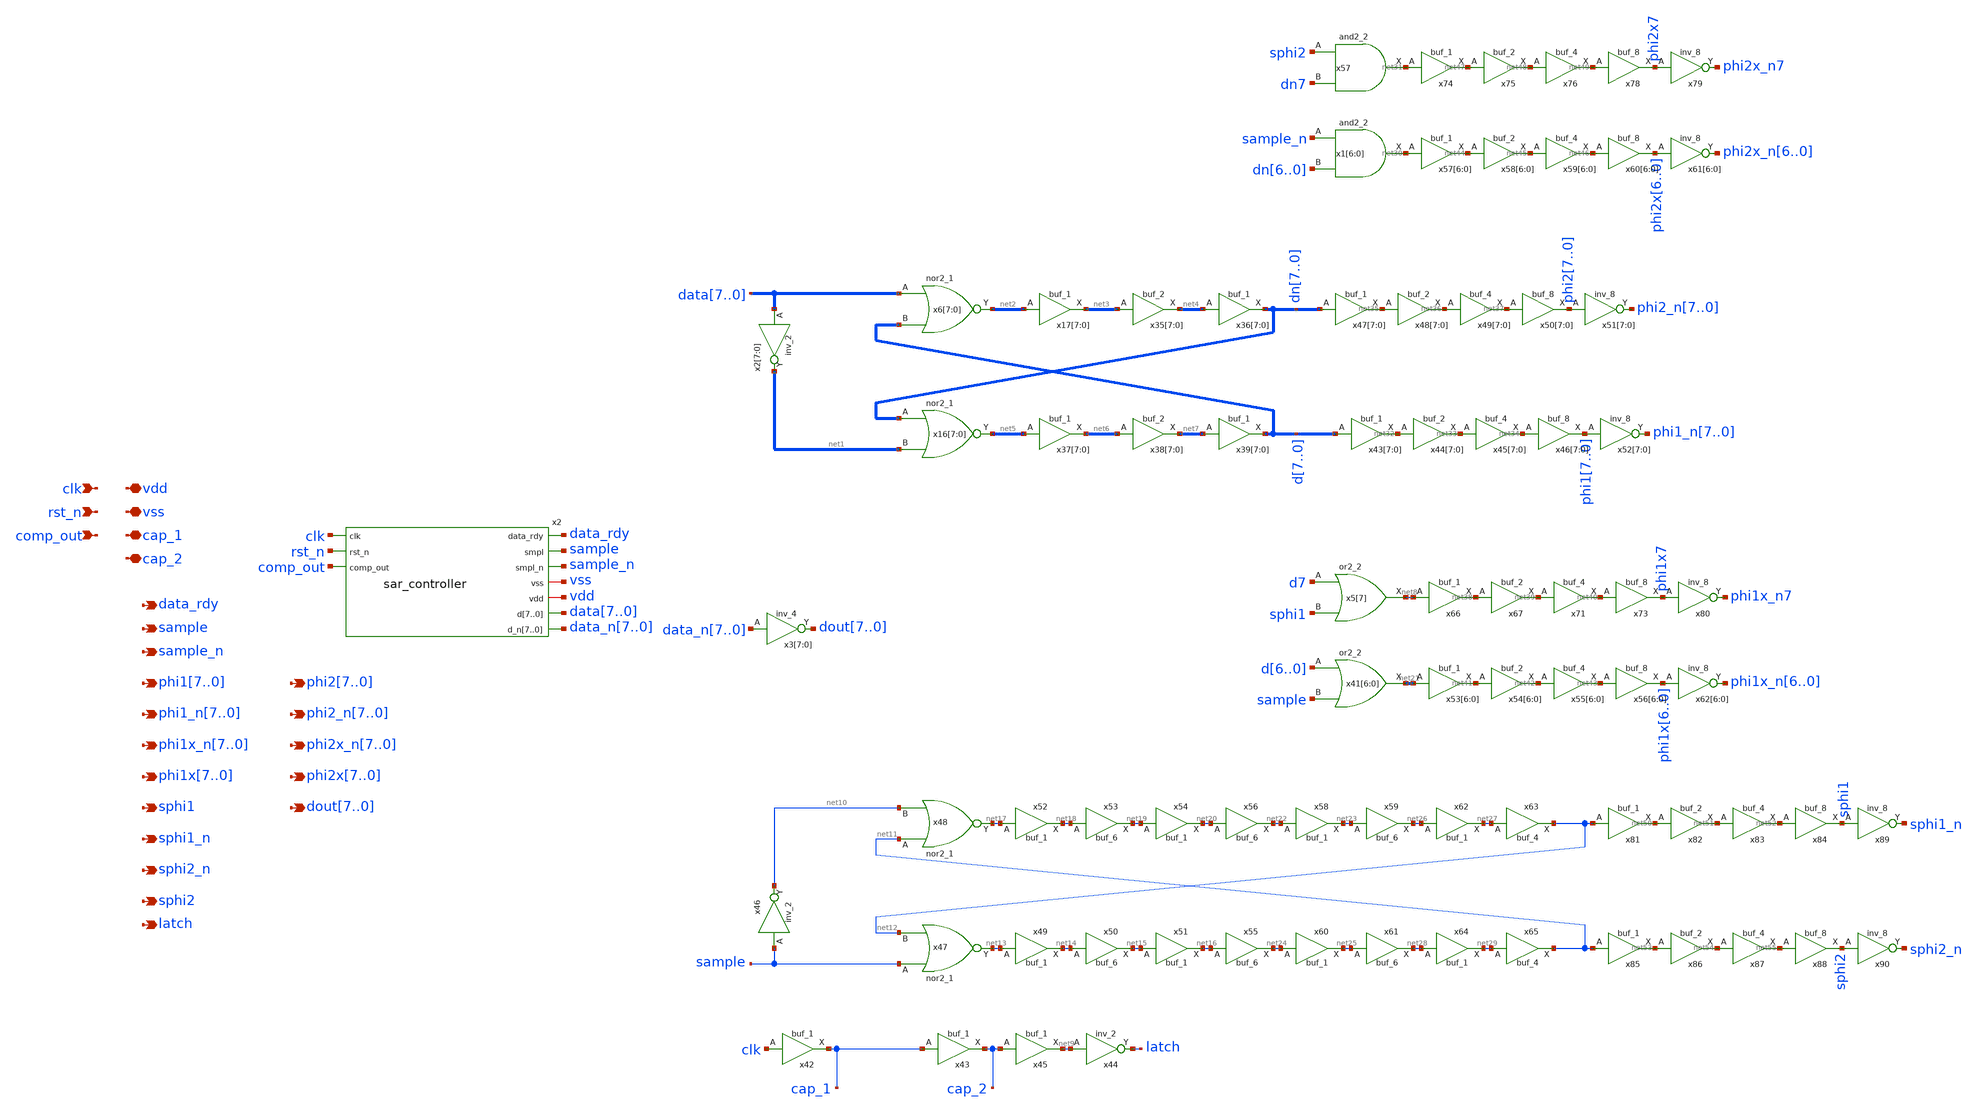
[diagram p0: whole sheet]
** sch_path: test/design/sar_digital.sch
**.subckt sar_digital data_rdy vss vdd clk rst_n comp_out sample sample_n cap_1 cap_2
*+ phi17,phi16,phi15,phi14,phi13,phi12,phi11,phi10 phi1_n7,phi1_n6,phi1_n5,phi1_n4,phi1_n3,phi1_n2,phi1_n1,phi1_n0
*+ phi1x_n7,phi1x_n6,phi1x_n5,phi1x_n4,phi1x_n3,phi1x_n2,phi1x_n1,phi1x_n0 phi1x7,phi1x6,phi1x5,phi1x4,phi1x3,phi1x2,phi1x1,phi1x0 sphi1 sphi1_n sphi2_n sphi2
*+ phi27,phi26,phi25,phi24,phi23,phi22,phi21,phi20 phi2_n7,phi2_n6,phi2_n5,phi2_n4,phi2_n3,phi2_n2,phi2_n1,phi2_n0
*+ phi2x_n7,phi2x_n6,phi2x_n5,phi2x_n4,phi2x_n3,phi2x_n2,phi2x_n1,phi2x_n0 phi2x7,phi2x6,phi2x5,phi2x4,phi2x3,phi2x2,phi2x1,phi2x0 latch
*+ dout7,dout6,dout5,dout4,dout3,dout2,dout1,dout0
*.opin data_rdy
*.iopin vss
*.iopin vdd
*.ipin clk
*.ipin rst_n
*.ipin comp_out
*.opin sample
*.opin sample_n
*.iopin cap_1
*.iopin cap_2
*.opin phi17,phi16,phi15,phi14,phi13,phi12,phi11,phi10
*.opin phi1_n7,phi1_n6,phi1_n5,phi1_n4,phi1_n3,phi1_n2,phi1_n1,phi1_n0
*.opin phi1x_n7,phi1x_n6,phi1x_n5,phi1x_n4,phi1x_n3,phi1x_n2,phi1x_n1,phi1x_n0
*.opin phi1x7,phi1x6,phi1x5,phi1x4,phi1x3,phi1x2,phi1x1,phi1x0
*.opin sphi1
*.opin sphi1_n
*.opin sphi2_n
*.opin sphi2
*.opin phi27,phi26,phi25,phi24,phi23,phi22,phi21,phi20
*.opin phi2_n7,phi2_n6,phi2_n5,phi2_n4,phi2_n3,phi2_n2,phi2_n1,phi2_n0
*.opin phi2x_n7,phi2x_n6,phi2x_n5,phi2x_n4,phi2x_n3,phi2x_n2,phi2x_n1,phi2x_n0
*.opin phi2x7,phi2x6,phi2x5,phi2x4,phi2x3,phi2x2,phi2x1,phi2x0
*.opin latch
*.opin dout7,dout6,dout5,dout4,dout3,dout2,dout1,dout0
x2 clk data_rdy sample rst_n sample_n comp_out vss vdd data7 data6 data5 data4 data3 data2 data1
+ data0 data_n7 data_n6 data_n5 data_n4 data_n3 data_n2 data_n1 data_n0 sar_controller
x2[7] data7 vss vss vdd vdd net1[7] sky130_fd_sc_hd__inv_2
x2[6] data6 vss vss vdd vdd net1[6] sky130_fd_sc_hd__inv_2
x2[5] data5 vss vss vdd vdd net1[5] sky130_fd_sc_hd__inv_2
x2[4] data4 vss vss vdd vdd net1[4] sky130_fd_sc_hd__inv_2
x2[3] data3 vss vss vdd vdd net1[3] sky130_fd_sc_hd__inv_2
x2[2] data2 vss vss vdd vdd net1[2] sky130_fd_sc_hd__inv_2
x2[1] data1 vss vss vdd vdd net1[1] sky130_fd_sc_hd__inv_2
x2[0] data0 vss vss vdd vdd net1[0] sky130_fd_sc_hd__inv_2
x6[7] data7 d7 vss vss vdd vdd net2[7] sky130_fd_sc_hd__nor2_1
x6[6] data6 d6 vss vss vdd vdd net2[6] sky130_fd_sc_hd__nor2_1
x6[5] data5 d5 vss vss vdd vdd net2[5] sky130_fd_sc_hd__nor2_1
x6[4] data4 d4 vss vss vdd vdd net2[4] sky130_fd_sc_hd__nor2_1
x6[3] data3 d3 vss vss vdd vdd net2[3] sky130_fd_sc_hd__nor2_1
x6[2] data2 d2 vss vss vdd vdd net2[2] sky130_fd_sc_hd__nor2_1
x6[1] data1 d1 vss vss vdd vdd net2[1] sky130_fd_sc_hd__nor2_1
x6[0] data0 d0 vss vss vdd vdd net2[0] sky130_fd_sc_hd__nor2_1
x16[7] dn7 net1[7] vss vss vdd vdd net5[7] sky130_fd_sc_hd__nor2_1
x16[6] dn6 net1[6] vss vss vdd vdd net5[6] sky130_fd_sc_hd__nor2_1
x16[5] dn5 net1[5] vss vss vdd vdd net5[5] sky130_fd_sc_hd__nor2_1
x16[4] dn4 net1[4] vss vss vdd vdd net5[4] sky130_fd_sc_hd__nor2_1
x16[3] dn3 net1[3] vss vss vdd vdd net5[3] sky130_fd_sc_hd__nor2_1
x16[2] dn2 net1[2] vss vss vdd vdd net5[2] sky130_fd_sc_hd__nor2_1
x16[1] dn1 net1[1] vss vss vdd vdd net5[1] sky130_fd_sc_hd__nor2_1
x16[0] dn0 net1[0] vss vss vdd vdd net5[0] sky130_fd_sc_hd__nor2_1
x17[7] net2[7] vss vss vdd vdd net3[7] sky130_fd_sc_hd__buf_1
x17[6] net2[6] vss vss vdd vdd net3[6] sky130_fd_sc_hd__buf_1
x17[5] net2[5] vss vss vdd vdd net3[5] sky130_fd_sc_hd__buf_1
x17[4] net2[4] vss vss vdd vdd net3[4] sky130_fd_sc_hd__buf_1
x17[3] net2[3] vss vss vdd vdd net3[3] sky130_fd_sc_hd__buf_1
x17[2] net2[2] vss vss vdd vdd net3[2] sky130_fd_sc_hd__buf_1
x17[1] net2[1] vss vss vdd vdd net3[1] sky130_fd_sc_hd__buf_1
x17[0] net2[0] vss vss vdd vdd net3[0] sky130_fd_sc_hd__buf_1
x35[7] net3[7] vss vss vdd vdd net4[7] sky130_fd_sc_hd__buf_2
x35[6] net3[6] vss vss vdd vdd net4[6] sky130_fd_sc_hd__buf_2
x35[5] net3[5] vss vss vdd vdd net4[5] sky130_fd_sc_hd__buf_2
x35[4] net3[4] vss vss vdd vdd net4[4] sky130_fd_sc_hd__buf_2
x35[3] net3[3] vss vss vdd vdd net4[3] sky130_fd_sc_hd__buf_2
x35[2] net3[2] vss vss vdd vdd net4[2] sky130_fd_sc_hd__buf_2
x35[1] net3[1] vss vss vdd vdd net4[1] sky130_fd_sc_hd__buf_2
x35[0] net3[0] vss vss vdd vdd net4[0] sky130_fd_sc_hd__buf_2
x36[7] net4[7] vss vss vdd vdd dn7 sky130_fd_sc_hd__buf_1
x36[6] net4[6] vss vss vdd vdd dn6 sky130_fd_sc_hd__buf_1
x36[5] net4[5] vss vss vdd vdd dn5 sky130_fd_sc_hd__buf_1
x36[4] net4[4] vss vss vdd vdd dn4 sky130_fd_sc_hd__buf_1
x36[3] net4[3] vss vss vdd vdd dn3 sky130_fd_sc_hd__buf_1
x36[2] net4[2] vss vss vdd vdd dn2 sky130_fd_sc_hd__buf_1
x36[1] net4[1] vss vss vdd vdd dn1 sky130_fd_sc_hd__buf_1
x36[0] net4[0] vss vss vdd vdd dn0 sky130_fd_sc_hd__buf_1
x37[7] net5[7] vss vss vdd vdd net6[7] sky130_fd_sc_hd__buf_1
x37[6] net5[6] vss vss vdd vdd net6[6] sky130_fd_sc_hd__buf_1
x37[5] net5[5] vss vss vdd vdd net6[5] sky130_fd_sc_hd__buf_1
x37[4] net5[4] vss vss vdd vdd net6[4] sky130_fd_sc_hd__buf_1
x37[3] net5[3] vss vss vdd vdd net6[3] sky130_fd_sc_hd__buf_1
x37[2] net5[2] vss vss vdd vdd net6[2] sky130_fd_sc_hd__buf_1
x37[1] net5[1] vss vss vdd vdd net6[1] sky130_fd_sc_hd__buf_1
x37[0] net5[0] vss vss vdd vdd net6[0] sky130_fd_sc_hd__buf_1
x38[7] net6[7] vss vss vdd vdd net7[7] sky130_fd_sc_hd__buf_2
x38[6] net6[6] vss vss vdd vdd net7[6] sky130_fd_sc_hd__buf_2
x38[5] net6[5] vss vss vdd vdd net7[5] sky130_fd_sc_hd__buf_2
x38[4] net6[4] vss vss vdd vdd net7[4] sky130_fd_sc_hd__buf_2
x38[3] net6[3] vss vss vdd vdd net7[3] sky130_fd_sc_hd__buf_2
x38[2] net6[2] vss vss vdd vdd net7[2] sky130_fd_sc_hd__buf_2
x38[1] net6[1] vss vss vdd vdd net7[1] sky130_fd_sc_hd__buf_2
x38[0] net6[0] vss vss vdd vdd net7[0] sky130_fd_sc_hd__buf_2
x39[7] net7[7] vss vss vdd vdd d7 sky130_fd_sc_hd__buf_1
x39[6] net7[6] vss vss vdd vdd d6 sky130_fd_sc_hd__buf_1
x39[5] net7[5] vss vss vdd vdd d5 sky130_fd_sc_hd__buf_1
x39[4] net7[4] vss vss vdd vdd d4 sky130_fd_sc_hd__buf_1
x39[3] net7[3] vss vss vdd vdd d3 sky130_fd_sc_hd__buf_1
x39[2] net7[2] vss vss vdd vdd d2 sky130_fd_sc_hd__buf_1
x39[1] net7[1] vss vss vdd vdd d1 sky130_fd_sc_hd__buf_1
x39[0] net7[0] vss vss vdd vdd d0 sky130_fd_sc_hd__buf_1
x5[7] d7 sphi1 vss vss vdd vdd net8 sky130_fd_sc_hd__or2_2
x1[6] sample_n dn6 vss vss vdd vdd net30[6] sky130_fd_sc_hd__and2_2
x1[5] sample_n dn5 vss vss vdd vdd net30[5] sky130_fd_sc_hd__and2_2
x1[4] sample_n dn4 vss vss vdd vdd net30[4] sky130_fd_sc_hd__and2_2
x1[3] sample_n dn3 vss vss vdd vdd net30[3] sky130_fd_sc_hd__and2_2
x1[2] sample_n dn2 vss vss vdd vdd net30[2] sky130_fd_sc_hd__and2_2
x1[1] sample_n dn1 vss vss vdd vdd net30[1] sky130_fd_sc_hd__and2_2
x1[0] sample_n dn0 vss vss vdd vdd net30[0] sky130_fd_sc_hd__and2_2
x42 clk vss vss vdd vdd cap_1 sky130_fd_sc_hd__buf_1
x43 cap_1 vss vss vdd vdd cap_2 sky130_fd_sc_hd__buf_1
x44 net9 vss vss vdd vdd latch sky130_fd_sc_hd__inv_2
x45 cap_2 vss vss vdd vdd net9 sky130_fd_sc_hd__buf_1
x46 sample vss vss vdd vdd net10 sky130_fd_sc_hd__inv_2
x47 sample net12 vss vss vdd vdd net13 sky130_fd_sc_hd__nor2_1
x48 net11 net10 vss vss vdd vdd net17 sky130_fd_sc_hd__nor2_1
x49 net13 vss vss vdd vdd net14 sky130_fd_sc_hd__buf_1
x50 net14 vss vss vdd vdd net15 sky130_fd_sc_hd__buf_6
x51 net15 vss vss vdd vdd net16 sky130_fd_sc_hd__buf_1
x52 net17 vss vss vdd vdd net18 sky130_fd_sc_hd__buf_1
x53 net18 vss vss vdd vdd net19 sky130_fd_sc_hd__buf_6
x54 net19 vss vss vdd vdd net20 sky130_fd_sc_hd__buf_1
x55 net16 vss vss vdd vdd net24 sky130_fd_sc_hd__buf_6
x56 net20 vss vss vdd vdd net22 sky130_fd_sc_hd__buf_6
x41[6] d6 sample vss vss vdd vdd net21[6] sky130_fd_sc_hd__or2_2
x41[5] d5 sample vss vss vdd vdd net21[5] sky130_fd_sc_hd__or2_2
x41[4] d4 sample vss vss vdd vdd net21[4] sky130_fd_sc_hd__or2_2
x41[3] d3 sample vss vss vdd vdd net21[3] sky130_fd_sc_hd__or2_2
x41[2] d2 sample vss vss vdd vdd net21[2] sky130_fd_sc_hd__or2_2
x41[1] d1 sample vss vss vdd vdd net21[1] sky130_fd_sc_hd__or2_2
x41[0] d0 sample vss vss vdd vdd net21[0] sky130_fd_sc_hd__or2_2
x57 sphi2 dn7 vss vss vdd vdd net31 sky130_fd_sc_hd__and2_2
x58 net22 vss vss vdd vdd net23 sky130_fd_sc_hd__buf_1
x59 net23 vss vss vdd vdd net26 sky130_fd_sc_hd__buf_6
x60 net24 vss vss vdd vdd net25 sky130_fd_sc_hd__buf_1
x61 net25 vss vss vdd vdd net28 sky130_fd_sc_hd__buf_6
x62 net26 vss vss vdd vdd net27 sky130_fd_sc_hd__buf_1
x63 net27 vss vss vdd vdd net12 sky130_fd_sc_hd__buf_4
x64 net28 vss vss vdd vdd net29 sky130_fd_sc_hd__buf_1
x65 net29 vss vss vdd vdd net11 sky130_fd_sc_hd__buf_4
x43[7] d7 vss vss vdd vdd net32[7] sky130_fd_sc_hd__buf_1
x43[6] d6 vss vss vdd vdd net32[6] sky130_fd_sc_hd__buf_1
x43[5] d5 vss vss vdd vdd net32[5] sky130_fd_sc_hd__buf_1
x43[4] d4 vss vss vdd vdd net32[4] sky130_fd_sc_hd__buf_1
x43[3] d3 vss vss vdd vdd net32[3] sky130_fd_sc_hd__buf_1
x43[2] d2 vss vss vdd vdd net32[2] sky130_fd_sc_hd__buf_1
x43[1] d1 vss vss vdd vdd net32[1] sky130_fd_sc_hd__buf_1
x43[0] d0 vss vss vdd vdd net32[0] sky130_fd_sc_hd__buf_1
x44[7] net32[7] vss vss vdd vdd net33[7] sky130_fd_sc_hd__buf_2
x44[6] net32[6] vss vss vdd vdd net33[6] sky130_fd_sc_hd__buf_2
x44[5] net32[5] vss vss vdd vdd net33[5] sky130_fd_sc_hd__buf_2
x44[4] net32[4] vss vss vdd vdd net33[4] sky130_fd_sc_hd__buf_2
x44[3] net32[3] vss vss vdd vdd net33[3] sky130_fd_sc_hd__buf_2
x44[2] net32[2] vss vss vdd vdd net33[2] sky130_fd_sc_hd__buf_2
x44[1] net32[1] vss vss vdd vdd net33[1] sky130_fd_sc_hd__buf_2
x44[0] net32[0] vss vss vdd vdd net33[0] sky130_fd_sc_hd__buf_2
x45[7] net33[7] vss vss vdd vdd net34[7] sky130_fd_sc_hd__buf_4
x45[6] net33[6] vss vss vdd vdd net34[6] sky130_fd_sc_hd__buf_4
x45[5] net33[5] vss vss vdd vdd net34[5] sky130_fd_sc_hd__buf_4
x45[4] net33[4] vss vss vdd vdd net34[4] sky130_fd_sc_hd__buf_4
x45[3] net33[3] vss vss vdd vdd net34[3] sky130_fd_sc_hd__buf_4
x45[2] net33[2] vss vss vdd vdd net34[2] sky130_fd_sc_hd__buf_4
x45[1] net33[1] vss vss vdd vdd net34[1] sky130_fd_sc_hd__buf_4
x45[0] net33[0] vss vss vdd vdd net34[0] sky130_fd_sc_hd__buf_4
x46[7] net34[7] vss vss vdd vdd phi17 sky130_fd_sc_hd__buf_8
x46[6] net34[6] vss vss vdd vdd phi16 sky130_fd_sc_hd__buf_8
x46[5] net34[5] vss vss vdd vdd phi15 sky130_fd_sc_hd__buf_8
x46[4] net34[4] vss vss vdd vdd phi14 sky130_fd_sc_hd__buf_8
x46[3] net34[3] vss vss vdd vdd phi13 sky130_fd_sc_hd__buf_8
x46[2] net34[2] vss vss vdd vdd phi12 sky130_fd_sc_hd__buf_8
x46[1] net34[1] vss vss vdd vdd phi11 sky130_fd_sc_hd__buf_8
x46[0] net34[0] vss vss vdd vdd phi10 sky130_fd_sc_hd__buf_8
x47[7] dn7 vss vss vdd vdd net35[7] sky130_fd_sc_hd__buf_1
x47[6] dn6 vss vss vdd vdd net35[6] sky130_fd_sc_hd__buf_1
x47[5] dn5 vss vss vdd vdd net35[5] sky130_fd_sc_hd__buf_1
x47[4] dn4 vss vss vdd vdd net35[4] sky130_fd_sc_hd__buf_1
x47[3] dn3 vss vss vdd vdd net35[3] sky130_fd_sc_hd__buf_1
x47[2] dn2 vss vss vdd vdd net35[2] sky130_fd_sc_hd__buf_1
x47[1] dn1 vss vss vdd vdd net35[1] sky130_fd_sc_hd__buf_1
x47[0] dn0 vss vss vdd vdd net35[0] sky130_fd_sc_hd__buf_1
x48[7] net35[7] vss vss vdd vdd net36[7] sky130_fd_sc_hd__buf_2
x48[6] net35[6] vss vss vdd vdd net36[6] sky130_fd_sc_hd__buf_2
x48[5] net35[5] vss vss vdd vdd net36[5] sky130_fd_sc_hd__buf_2
x48[4] net35[4] vss vss vdd vdd net36[4] sky130_fd_sc_hd__buf_2
x48[3] net35[3] vss vss vdd vdd net36[3] sky130_fd_sc_hd__buf_2
x48[2] net35[2] vss vss vdd vdd net36[2] sky130_fd_sc_hd__buf_2
x48[1] net35[1] vss vss vdd vdd net36[1] sky130_fd_sc_hd__buf_2
x48[0] net35[0] vss vss vdd vdd net36[0] sky130_fd_sc_hd__buf_2
x49[7] net36[7] vss vss vdd vdd net37[7] sky130_fd_sc_hd__buf_4
x49[6] net36[6] vss vss vdd vdd net37[6] sky130_fd_sc_hd__buf_4
x49[5] net36[5] vss vss vdd vdd net37[5] sky130_fd_sc_hd__buf_4
x49[4] net36[4] vss vss vdd vdd net37[4] sky130_fd_sc_hd__buf_4
x49[3] net36[3] vss vss vdd vdd net37[3] sky130_fd_sc_hd__buf_4
x49[2] net36[2] vss vss vdd vdd net37[2] sky130_fd_sc_hd__buf_4
x49[1] net36[1] vss vss vdd vdd net37[1] sky130_fd_sc_hd__buf_4
x49[0] net36[0] vss vss vdd vdd net37[0] sky130_fd_sc_hd__buf_4
x50[7] net37[7] vss vss vdd vdd phi27 sky130_fd_sc_hd__buf_8
x50[6] net37[6] vss vss vdd vdd phi26 sky130_fd_sc_hd__buf_8
x50[5] net37[5] vss vss vdd vdd phi25 sky130_fd_sc_hd__buf_8
x50[4] net37[4] vss vss vdd vdd phi24 sky130_fd_sc_hd__buf_8
x50[3] net37[3] vss vss vdd vdd phi23 sky130_fd_sc_hd__buf_8
x50[2] net37[2] vss vss vdd vdd phi22 sky130_fd_sc_hd__buf_8
x50[1] net37[1] vss vss vdd vdd phi21 sky130_fd_sc_hd__buf_8
x50[0] net37[0] vss vss vdd vdd phi20 sky130_fd_sc_hd__buf_8
x51[7] phi27 vss vss vdd vdd phi2_n7 sky130_fd_sc_hd__inv_8
x51[6] phi26 vss vss vdd vdd phi2_n6 sky130_fd_sc_hd__inv_8
x51[5] phi25 vss vss vdd vdd phi2_n5 sky130_fd_sc_hd__inv_8
x51[4] phi24 vss vss vdd vdd phi2_n4 sky130_fd_sc_hd__inv_8
x51[3] phi23 vss vss vdd vdd phi2_n3 sky130_fd_sc_hd__inv_8
x51[2] phi22 vss vss vdd vdd phi2_n2 sky130_fd_sc_hd__inv_8
x51[1] phi21 vss vss vdd vdd phi2_n1 sky130_fd_sc_hd__inv_8
x51[0] phi20 vss vss vdd vdd phi2_n0 sky130_fd_sc_hd__inv_8
x52[7] phi17 vss vss vdd vdd phi1_n7 sky130_fd_sc_hd__inv_8
x52[6] phi16 vss vss vdd vdd phi1_n6 sky130_fd_sc_hd__inv_8
x52[5] phi15 vss vss vdd vdd phi1_n5 sky130_fd_sc_hd__inv_8
x52[4] phi14 vss vss vdd vdd phi1_n4 sky130_fd_sc_hd__inv_8
x52[3] phi13 vss vss vdd vdd phi1_n3 sky130_fd_sc_hd__inv_8
x52[2] phi12 vss vss vdd vdd phi1_n2 sky130_fd_sc_hd__inv_8
x52[1] phi11 vss vss vdd vdd phi1_n1 sky130_fd_sc_hd__inv_8
x52[0] phi10 vss vss vdd vdd phi1_n0 sky130_fd_sc_hd__inv_8
x66 net8 vss vss vdd vdd net38 sky130_fd_sc_hd__buf_1
x67 net38 vss vss vdd vdd net39 sky130_fd_sc_hd__buf_2
x71 net39 vss vss vdd vdd net40 sky130_fd_sc_hd__buf_4
x73 net40 vss vss vdd vdd phi1x7 sky130_fd_sc_hd__buf_8
x53[6] net21[6] vss vss vdd vdd net41[6] sky130_fd_sc_hd__buf_1
x53[5] net21[5] vss vss vdd vdd net41[5] sky130_fd_sc_hd__buf_1
x53[4] net21[4] vss vss vdd vdd net41[4] sky130_fd_sc_hd__buf_1
x53[3] net21[3] vss vss vdd vdd net41[3] sky130_fd_sc_hd__buf_1
x53[2] net21[2] vss vss vdd vdd net41[2] sky130_fd_sc_hd__buf_1
x53[1] net21[1] vss vss vdd vdd net41[1] sky130_fd_sc_hd__buf_1
x53[0] net21[0] vss vss vdd vdd net41[0] sky130_fd_sc_hd__buf_1
x54[6] net41[6] vss vss vdd vdd net42[6] sky130_fd_sc_hd__buf_2
x54[5] net41[5] vss vss vdd vdd net42[5] sky130_fd_sc_hd__buf_2
x54[4] net41[4] vss vss vdd vdd net42[4] sky130_fd_sc_hd__buf_2
x54[3] net41[3] vss vss vdd vdd net42[3] sky130_fd_sc_hd__buf_2
x54[2] net41[2] vss vss vdd vdd net42[2] sky130_fd_sc_hd__buf_2
x54[1] net41[1] vss vss vdd vdd net42[1] sky130_fd_sc_hd__buf_2
x54[0] net41[0] vss vss vdd vdd net42[0] sky130_fd_sc_hd__buf_2
x55[6] net42[6] vss vss vdd vdd net43[6] sky130_fd_sc_hd__buf_4
x55[5] net42[5] vss vss vdd vdd net43[5] sky130_fd_sc_hd__buf_4
x55[4] net42[4] vss vss vdd vdd net43[4] sky130_fd_sc_hd__buf_4
x55[3] net42[3] vss vss vdd vdd net43[3] sky130_fd_sc_hd__buf_4
x55[2] net42[2] vss vss vdd vdd net43[2] sky130_fd_sc_hd__buf_4
x55[1] net42[1] vss vss vdd vdd net43[1] sky130_fd_sc_hd__buf_4
x55[0] net42[0] vss vss vdd vdd net43[0] sky130_fd_sc_hd__buf_4
x56[6] net43[6] vss vss vdd vdd phi1x6 sky130_fd_sc_hd__buf_8
x56[5] net43[5] vss vss vdd vdd phi1x5 sky130_fd_sc_hd__buf_8
x56[4] net43[4] vss vss vdd vdd phi1x4 sky130_fd_sc_hd__buf_8
x56[3] net43[3] vss vss vdd vdd phi1x3 sky130_fd_sc_hd__buf_8
x56[2] net43[2] vss vss vdd vdd phi1x2 sky130_fd_sc_hd__buf_8
x56[1] net43[1] vss vss vdd vdd phi1x1 sky130_fd_sc_hd__buf_8
x56[0] net43[0] vss vss vdd vdd phi1x0 sky130_fd_sc_hd__buf_8
x57[6] net30[6] vss vss vdd vdd net44[6] sky130_fd_sc_hd__buf_1
x57[5] net30[5] vss vss vdd vdd net44[5] sky130_fd_sc_hd__buf_1
x57[4] net30[4] vss vss vdd vdd net44[4] sky130_fd_sc_hd__buf_1
x57[3] net30[3] vss vss vdd vdd net44[3] sky130_fd_sc_hd__buf_1
x57[2] net30[2] vss vss vdd vdd net44[2] sky130_fd_sc_hd__buf_1
x57[1] net30[1] vss vss vdd vdd net44[1] sky130_fd_sc_hd__buf_1
x57[0] net30[0] vss vss vdd vdd net44[0] sky130_fd_sc_hd__buf_1
x58[6] net44[6] vss vss vdd vdd net45[6] sky130_fd_sc_hd__buf_2
x58[5] net44[5] vss vss vdd vdd net45[5] sky130_fd_sc_hd__buf_2
x58[4] net44[4] vss vss vdd vdd net45[4] sky130_fd_sc_hd__buf_2
x58[3] net44[3] vss vss vdd vdd net45[3] sky130_fd_sc_hd__buf_2
x58[2] net44[2] vss vss vdd vdd net45[2] sky130_fd_sc_hd__buf_2
x58[1] net44[1] vss vss vdd vdd net45[1] sky130_fd_sc_hd__buf_2
x58[0] net44[0] vss vss vdd vdd net45[0] sky130_fd_sc_hd__buf_2
x59[6] net45[6] vss vss vdd vdd net46[6] sky130_fd_sc_hd__buf_4
x59[5] net45[5] vss vss vdd vdd net46[5] sky130_fd_sc_hd__buf_4
x59[4] net45[4] vss vss vdd vdd net46[4] sky130_fd_sc_hd__buf_4
x59[3] net45[3] vss vss vdd vdd net46[3] sky130_fd_sc_hd__buf_4
x59[2] net45[2] vss vss vdd vdd net46[2] sky130_fd_sc_hd__buf_4
x59[1] net45[1] vss vss vdd vdd net46[1] sky130_fd_sc_hd__buf_4
x59[0] net45[0] vss vss vdd vdd net46[0] sky130_fd_sc_hd__buf_4
x60[6] net46[6] vss vss vdd vdd phi2x6 sky130_fd_sc_hd__buf_8
x60[5] net46[5] vss vss vdd vdd phi2x5 sky130_fd_sc_hd__buf_8
x60[4] net46[4] vss vss vdd vdd phi2x4 sky130_fd_sc_hd__buf_8
x60[3] net46[3] vss vss vdd vdd phi2x3 sky130_fd_sc_hd__buf_8
x60[2] net46[2] vss vss vdd vdd phi2x2 sky130_fd_sc_hd__buf_8
x60[1] net46[1] vss vss vdd vdd phi2x1 sky130_fd_sc_hd__buf_8
x60[0] net46[0] vss vss vdd vdd phi2x0 sky130_fd_sc_hd__buf_8
x74 net31 vss vss vdd vdd net47 sky130_fd_sc_hd__buf_1
x75 net47 vss vss vdd vdd net48 sky130_fd_sc_hd__buf_2
x76 net48 vss vss vdd vdd net49 sky130_fd_sc_hd__buf_4
x78 net49 vss vss vdd vdd phi2x7 sky130_fd_sc_hd__buf_8
x79 phi2x7 vss vss vdd vdd phi2x_n7 sky130_fd_sc_hd__inv_8
x61[6] phi2x6 vss vss vdd vdd phi2x_n6 sky130_fd_sc_hd__inv_8
x61[5] phi2x5 vss vss vdd vdd phi2x_n5 sky130_fd_sc_hd__inv_8
x61[4] phi2x4 vss vss vdd vdd phi2x_n4 sky130_fd_sc_hd__inv_8
x61[3] phi2x3 vss vss vdd vdd phi2x_n3 sky130_fd_sc_hd__inv_8
x61[2] phi2x2 vss vss vdd vdd phi2x_n2 sky130_fd_sc_hd__inv_8
x61[1] phi2x1 vss vss vdd vdd phi2x_n1 sky130_fd_sc_hd__inv_8
x61[0] phi2x0 vss vss vdd vdd phi2x_n0 sky130_fd_sc_hd__inv_8
x80 phi1x7 vss vss vdd vdd phi1x_n7 sky130_fd_sc_hd__inv_8
x62[6] phi1x6 vss vss vdd vdd phi1x_n6 sky130_fd_sc_hd__inv_8
x62[5] phi1x5 vss vss vdd vdd phi1x_n5 sky130_fd_sc_hd__inv_8
x62[4] phi1x4 vss vss vdd vdd phi1x_n4 sky130_fd_sc_hd__inv_8
x62[3] phi1x3 vss vss vdd vdd phi1x_n3 sky130_fd_sc_hd__inv_8
x62[2] phi1x2 vss vss vdd vdd phi1x_n2 sky130_fd_sc_hd__inv_8
x62[1] phi1x1 vss vss vdd vdd phi1x_n1 sky130_fd_sc_hd__inv_8
x62[0] phi1x0 vss vss vdd vdd phi1x_n0 sky130_fd_sc_hd__inv_8
x81 net12 vss vss vdd vdd net50 sky130_fd_sc_hd__buf_1
x82 net50 vss vss vdd vdd net51 sky130_fd_sc_hd__buf_2
x83 net51 vss vss vdd vdd net52 sky130_fd_sc_hd__buf_4
x84 net52 vss vss vdd vdd sphi1 sky130_fd_sc_hd__buf_8
x85 net11 vss vss vdd vdd net53 sky130_fd_sc_hd__buf_1
x86 net53 vss vss vdd vdd net54 sky130_fd_sc_hd__buf_2
x87 net54 vss vss vdd vdd net55 sky130_fd_sc_hd__buf_4
x88 net55 vss vss vdd vdd sphi2 sky130_fd_sc_hd__buf_8
x89 sphi1 vss vss vdd vdd sphi1_n sky130_fd_sc_hd__inv_8
x90 sphi2 vss vss vdd vdd sphi2_n sky130_fd_sc_hd__inv_8
x3[7] data_n7 vss vss vdd vdd dout7 sky130_fd_sc_hd__inv_4
x3[6] data_n6 vss vss vdd vdd dout6 sky130_fd_sc_hd__inv_4
x3[5] data_n5 vss vss vdd vdd dout5 sky130_fd_sc_hd__inv_4
x3[4] data_n4 vss vss vdd vdd dout4 sky130_fd_sc_hd__inv_4
x3[3] data_n3 vss vss vdd vdd dout3 sky130_fd_sc_hd__inv_4
x3[2] data_n2 vss vss vdd vdd dout2 sky130_fd_sc_hd__inv_4
x3[1] data_n1 vss vss vdd vdd dout1 sky130_fd_sc_hd__inv_4
x3[0] data_n0 vss vss vdd vdd dout0 sky130_fd_sc_hd__inv_4
**.ends

* expanding   symbol:  /foss/designs/test/design/sar_controller.sym # of pins=10
** sym_path: test/design/sar_controller.sym
** sch_path: test/design/sar_controller.sch
.subckt sar_controller clk data_rdy smpl rst_n smpl_n comp_out vss vdd d7 d6 d5 d4 d3 d2 d1 d0 d_n7
+ d_n6 d_n5 d_n4 d_n3 d_n2 d_n1 d_n0
*.ipin rst_n
*.opin data_rdy
*.ipin clk
*.opin smpl
*.ipin comp_out
*.iopin vss
*.iopin vdd
*.opin d7,d6,d5,d4,d3,d2,d1,d0
*.opin d_n7,d_n6,d_n5,d_n4,d_n3,d_n2,d_n1,d_n0
*.opin smpl_n
x26 net2 net21 net22 net9 vss vss vdd vdd net1 net25 sky130_fd_sc_hd__dfbbp_1
x5 net19 net23 net20 vss vss vdd vdd cnv_7 net9 sky130_fd_sc_hd__dfrbp_1
* noconn #net33
x24 net19 net8 net20 vss vss vdd vdd net23 net24 sky130_fd_sc_hd__dfsbp_1
x6 net24 net20 vss vss vdd vdd net22 sky130_fd_sc_hd__and2_4
x1 net19 cnv_7 net20 vss vss vdd vdd cnv_6 net12 sky130_fd_sc_hd__dfrbp_1
x2 net19 cnv_6 net20 vss vss vdd vdd cnv_5 net13 sky130_fd_sc_hd__dfrbp_1
x3 net19 cnv_5 net20 vss vss vdd vdd cnv_4 net14 sky130_fd_sc_hd__dfrbp_1
x4 net19 cnv_4 net20 vss vss vdd vdd cnv_3 net15 sky130_fd_sc_hd__dfrbp_1
x7 net19 cnv_3 net20 vss vss vdd vdd cnv_2 net16 sky130_fd_sc_hd__dfrbp_1
x8 net19 cnv_2 net20 vss vss vdd vdd cnv_1 net17 sky130_fd_sc_hd__dfrbp_1
x9 net19 cnv_1 net20 vss vss vdd vdd cnv_0 net18 sky130_fd_sc_hd__dfrbp_1
x10 net19 cnv_0 net20 vss vss vdd vdd net8 net33 sky130_fd_sc_hd__dfrbp_1
x11 vss vss net22 vss vss vdd vdd net11 net34 sky130_fd_sc_hd__dfrbp_1
x12 net10 net21 net22 net12 vss vss vdd vdd net2 net26 sky130_fd_sc_hd__dfbbp_1
x13 net3 net21 net22 net13 vss vss vdd vdd net10 net27 sky130_fd_sc_hd__dfbbp_1
x14 net4 net21 net22 net14 vss vss vdd vdd net3 net28 sky130_fd_sc_hd__dfbbp_1
x15 net5 net21 net22 net15 vss vss vdd vdd net4 net29 sky130_fd_sc_hd__dfbbp_1
x16 net6 net21 net22 net16 vss vss vdd vdd net5 net30 sky130_fd_sc_hd__dfbbp_1
x17 net7 net21 net22 net17 vss vss vdd vdd net6 net31 sky130_fd_sc_hd__dfbbp_1
x18 net11 net21 net22 net18 vss vss vdd vdd net7 net32 sky130_fd_sc_hd__dfbbp_1
* noconn #net34
x19 net1 vss vss vdd vdd d7 sky130_fd_sc_hd__buf_2
x20 net25 vss vss vdd vdd d_n7 sky130_fd_sc_hd__buf_2
x21 net2 vss vss vdd vdd d6 sky130_fd_sc_hd__buf_2
x22 net26 vss vss vdd vdd d_n6 sky130_fd_sc_hd__buf_2
x23 net10 vss vss vdd vdd d5 sky130_fd_sc_hd__buf_2
x25 net27 vss vss vdd vdd d_n5 sky130_fd_sc_hd__buf_2
x27 net3 vss vss vdd vdd d4 sky130_fd_sc_hd__buf_2
x28 net28 vss vss vdd vdd d_n4 sky130_fd_sc_hd__buf_2
x29 net4 vss vss vdd vdd d3 sky130_fd_sc_hd__buf_2
x30 net29 vss vss vdd vdd d_n3 sky130_fd_sc_hd__buf_2
x31 net5 vss vss vdd vdd d2 sky130_fd_sc_hd__buf_2
x32 net30 vss vss vdd vdd d_n2 sky130_fd_sc_hd__buf_2
x33 net6 vss vss vdd vdd d1 sky130_fd_sc_hd__buf_2
x34 net31 vss vss vdd vdd d_n1 sky130_fd_sc_hd__buf_2
x35 net7 vss vss vdd vdd d0 sky130_fd_sc_hd__buf_2
x36 net32 vss vss vdd vdd d_n0 sky130_fd_sc_hd__buf_2
x37 net23 vss vss vdd vdd smpl sky130_fd_sc_hd__buf_2
x38 net24 vss vss vdd vdd smpl_n sky130_fd_sc_hd__buf_2
x39 net8 vss vss vdd vdd data_rdy sky130_fd_sc_hd__buf_2
x40 comp_out vss vss vdd vdd net21 sky130_fd_sc_hd__buf_4
x41 rst_n vss vss vdd vdd net20 sky130_fd_sc_hd__buf_4
x42 clk vss vss vdd vdd net19 sky130_fd_sc_hd__buf_4
.ends

.end
